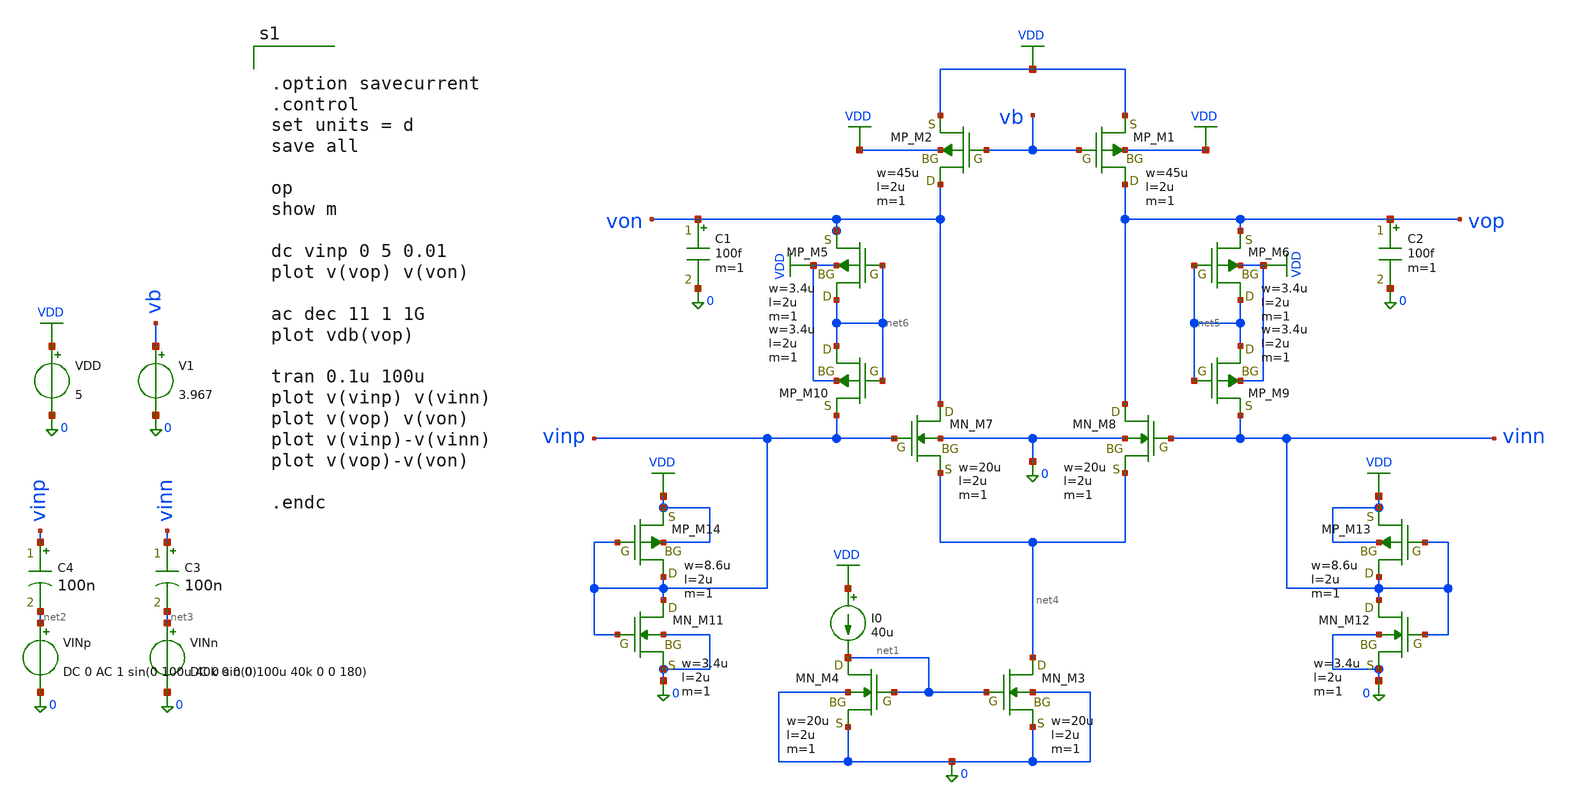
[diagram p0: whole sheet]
** sch_path: member_project/JJY_Receiver/Masahiro/jjy_recv/diff_amp/diff_nin_res.sch
**.subckt diff_nin_res
VDD VDD 0 5
VINp net2 0 DC 0 AC 1 sin(0 100u 40k 0 0 0)
I0 VDD net1 40u
C1 von 0 100f m=1
V1 vb 0 3.967
XM1 vop vb VDD VDD PMOS w=45u l=2u as=0 ad=0 ps=0 pd=0 nrd=0 nrs=0 m=1
XM2 von vb VDD VDD PMOS w=45u l=2u as=0 ad=0 ps=0 pd=0 nrd=0 nrs=0 m=1
XM3 net4 net1 0 0 NMOS w=20u l=2u as=0 ad=0 ps=0 pd=0 nrd=0 nrs=0 m=1
XM4 net1 net1 0 0 NMOS w=20u l=2u as=0 ad=0 ps=0 pd=0 nrd=0 nrs=0 m=1
C2 vop 0 100f m=1
VINn net3 0 DC 0 sin(0 100u 40k 0 0 180)
XM7 von vinp net4 0 NMOS w=20u l=2u as=0 ad=0 ps=0 pd=0 nrd=0 nrs=0 m=1
XM8 vop vinn net4 0 NMOS w=20u l=2u as=0 ad=0 ps=0 pd=0 nrd=0 nrs=0 m=1
XM6 net5 net5 vop VDD PMOS w=3.4u l=2u as=0 ad=0 ps=0 pd=0 nrd=0 nrs=0 m=1
XM9 net5 net5 vinn VDD PMOS w=3.4u l=2u as=0 ad=0 ps=0 pd=0 nrd=0 nrs=0 m=1
XM5 net6 net6 von VDD PMOS w=3.4u l=2u as=0 ad=0 ps=0 pd=0 nrd=0 nrs=0 m=1
XM10 net6 net6 vinp VDD PMOS w=3.4u l=2u as=0 ad=0 ps=0 pd=0 nrd=0 nrs=0 m=1
C3 vinn net3 100n m=1
C4 vinp net2 100n m=1
XM12 vinn vinn 0 0 NMOS w=3.4u l=2u as=0 ad=0 ps=0 pd=0 nrd=0 nrs=0 m=1
XM13 vinn vinn VDD VDD PMOS w=8.6u l=2u as=0 ad=0 ps=0 pd=0 nrd=0 nrs=0 m=1
XM11 vinp vinp 0 0 NMOS w=3.4u l=2u as=0 ad=0 ps=0 pd=0 nrd=0 nrs=0 m=1
XM14 vinp vinp VDD VDD PMOS w=8.6u l=2u as=0 ad=0 ps=0 pd=0 nrd=0 nrs=0 m=1
**** begin user architecture code
 .include $::LIB/ip62_models


.option savecurrent
.control
set units = d
save all

op
show m

dc vinp 0 5 0.01
plot v(vop) v(von)

ac dec 11 1 1G
plot vdb(vop)

tran 0.1u 100u
plot v(vinp) v(vinn)
plot v(vop) v(von)
plot v(vinp)-v(vinn)
plot v(vop)-v(von)

.endc


**** end user architecture code
**.ends
.GLOBAL VDD
.end
